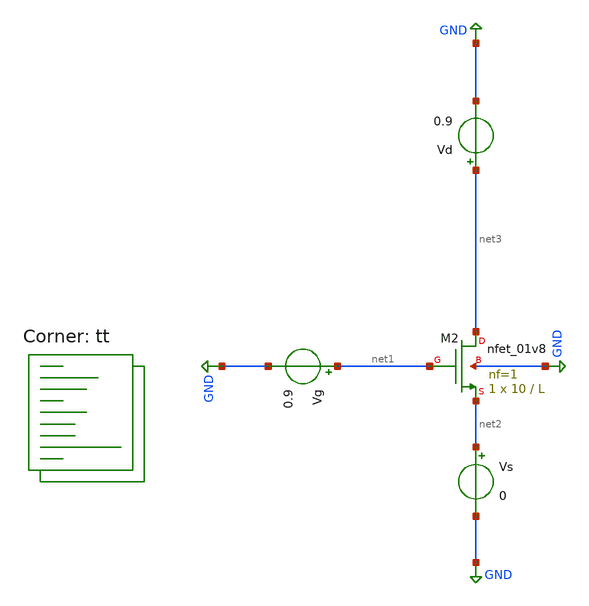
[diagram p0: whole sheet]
** sch_path: userLib/userLib/GmId.sch
**.subckt GmId
Vd net3 GND 0.9
Vg net1 GND 0.9
XM2 net3 net1 net2 GND sky130_fd_pr__nfet_01v8 L=L W=10 nf=1 ad='int((nf+1)/2) * W/nf * 0.29' as='int((nf+2)/2) * W/nf * 0.29'
+ pd='2*int((nf+1)/2) * (W/nf + 0.29)' ps='2*int((nf+2)/2) * (W/nf + 0.29)' nrd='0.29 / W' nrs='0.29 / W'
+ sa=0 sb=0 sd=0 mult=1 m=1
Vs net2 GND 0
**** begin user architecture code
.lib $::SKYWATER_MODELS/sky130.lib.spice tt

* this option enables mos model bin
* selection based on W/NF instead of W
.option wnflag=1
.option savecurrents

.param L=0.15
.param Vsb=0
.control
save all

let Lmax = 3
let Ldelta = 0.15;
let Lstart = 0.15;
let Lact = 0.15



save @m.xm2.msky130_fd_pr__nfet_01v8[id]
save @m.xm2.msky130_fd_pr__nfet_01v8[gm]
save @m.xm2.msky130_fd_pr__nfet_01v8[gds]
save @m.xm2.msky130_fd_pr__nfet_01v8[vth]
save @m.xm2.msky130_fd_pr__nfet_01v8[cgg]
save @m.xm2.msky130_fd_pr__nfet_01v8[vds]
save @m.xm2.msky130_fd_pr__nfet_01v8[vgs]
save @m.xm2.msky130_fd_pr__nfet_01v8[vbs]
save @m.xm2.msky130_fd_pr__nfet_01v8[l]

while Lact le Lmax
 echo L = $&Lact

  dc Vs 0 0.2 0.02
  let Lact = Lact + Ldelta
 alterparam L = Lact
end
  plot all.@m.xm2.msky130_fd_pr__nfet_01v8[gm]
  plot all.@m.xm2.msky130_fd_pr__nfet_01v8[gds]
  plot all.@m.xm2.msky130_fd_pr__nfet_01v8[vth]
  plot all.@m.xm2.msky130_fd_pr__nfet_01v8[cgg]
  plot all.@m.xm2.msky130_fd_pr__nfet_01v8[id]
  plot all.@m.xm2.msky130_fd_pr__nfet_01v8[vbs]
  set appendwrite
 set filetype=binary
 write GmId.raw

 set wr_singlescale
 set wr_vecnames
 wrdata GmIdvs.csv all.@m.xm2.msky130_fd_pr__nfet_01v8[id] all.@m.xm2.msky130_fd_pr__nfet_01v8[gm]
+  all.@m.xm2.msky130_fd_pr__nfet_01v8[gds] all.@m.xm2.msky130_fd_pr__nfet_01v8[cgg] all.@m.xm2.msky130_fd_pr__nfet_01v8[vgs]
+ all.@m.xm2.msky130_fd_pr__nfet_01v8[vds]  all.@m.xm2.msky130_fd_pr__nfet_01v8[vth]
.endc



**** end user architecture code
**.ends
.GLOBAL GND
.end
